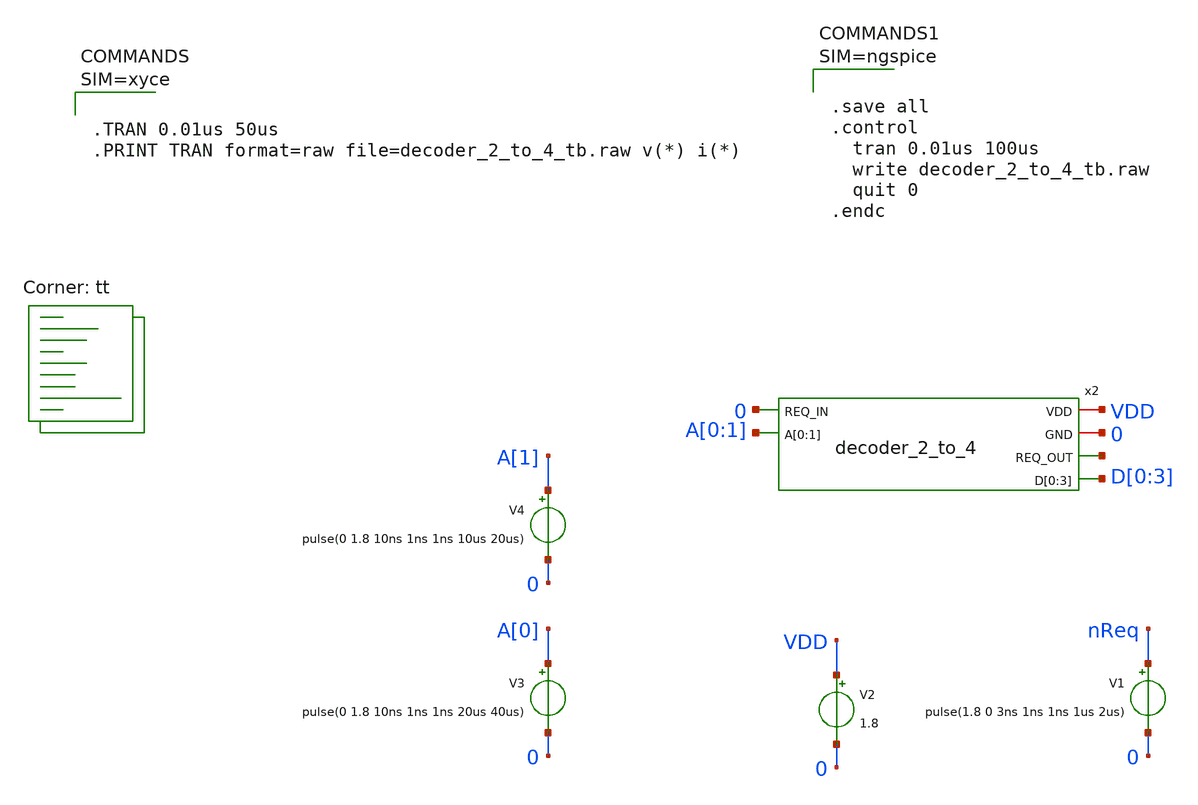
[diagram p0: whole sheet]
** sch_path: design/xschem/decoder_2_to_4_tb.sch
**.subckt decoder_2_to_4_tb
V3 A[0] 0 pulse(0 1.8 10ns 1ns 1ns 20us 40us)
V4 A[1] 0 pulse(0 1.8 10ns 1ns 1ns 10us 20us)
V2 VDD 0 1.8
V1 nReq 0 pulse(1.8 0 3ns 1ns 1ns 1us 2us)
x2 VDD 0 0 net1 A[0] A[1] D[0] D[1] D[2] D[3] decoder_2_to_4
**** begin user architecture code


* Standard cell simulation files
.include $::SKYWATER_STDCELLS/sky130_fd_sc_hd.spice


.lib $::SKYWATER_MODELS/sky130.lib.spice tt






.save all
.control
  tran 0.01us 100us
  write decoder_2_to_4_tb.raw
  quit 0
.endc



**** end user architecture code
**.ends

* expanding   symbol:  decoder_2_to_4.sym # of pins=6
** sym_path: design/xschem/decoder_2_to_4.sym
** sch_path: design/xschem/decoder_2_to_4.sch
.subckt decoder_2_to_4 VDD GND REQ_IN REQ_OUT A[0] A[1] D[0] D[1] D[2] D[3]
*.ipin A[0],A[1]
*.opin D[0],D[1],D[2],D[3]
*.ipin REQ_IN
*.opin REQ_OUT
*.iopin VDD
*.iopin GND
x3 A[0] GND GND VDD VDD net1 sky130_fd_sc_hd__inv_1
x7 A[1] GND GND VDD VDD net2 sky130_fd_sc_hd__inv_1
x1 net2 GND GND VDD VDD net4 sky130_fd_sc_hd__inv_1
x2 net1 GND GND VDD VDD net3 sky130_fd_sc_hd__inv_1
x10 net5 GND GND VDD VDD D[0] sky130_fd_sc_hd__inv_1
x11 net8 GND GND VDD VDD D[1] sky130_fd_sc_hd__inv_1
x12 net7 GND GND VDD VDD D[2] sky130_fd_sc_hd__inv_1
x13 net6 GND GND VDD VDD D[3] sky130_fd_sc_hd__inv_1
x4 net2 net3 GND GND VDD VDD net7 sky130_fd_sc_hd__nand2_1
x5 net4 net3 GND GND VDD VDD net6 sky130_fd_sc_hd__nand2_1
x6 net4 net1 GND GND VDD VDD net8 sky130_fd_sc_hd__nand2_1
x8 net2 net1 GND GND VDD VDD net5 sky130_fd_sc_hd__nand2_1
x9 REQ_IN GND GND VDD VDD net9 sky130_fd_sc_hd__inv_1
x14 net9 GND GND VDD VDD net10 sky130_fd_sc_hd__inv_1
x15 net10 GND GND VDD VDD net11 sky130_fd_sc_hd__inv_1
x16 net11 GND GND VDD VDD REQ_OUT sky130_fd_sc_hd__inv_1
.ends

.end
